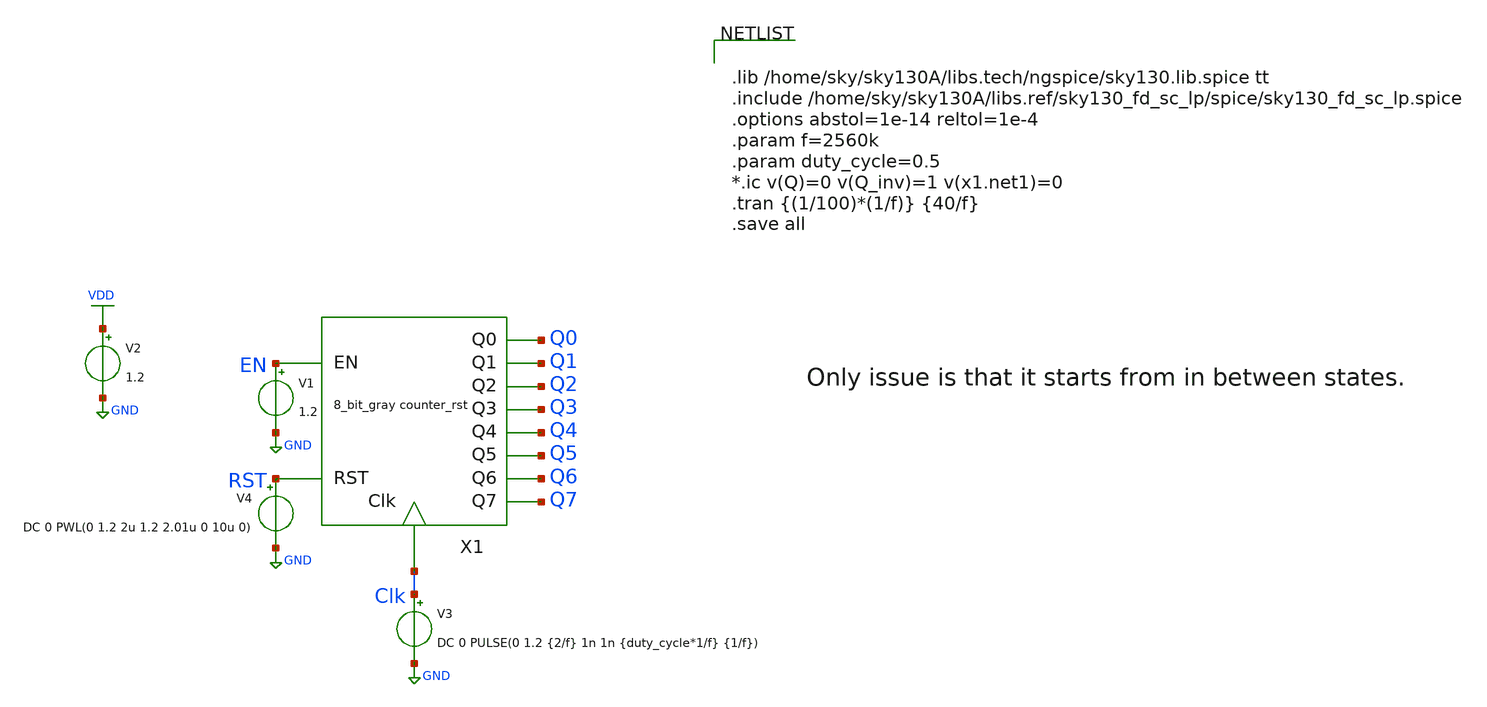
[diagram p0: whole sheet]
** sch_path: xschem/8_bit_gray_counter/8_bit_gray_counter_rst_tb.sch
**.subckt 8_bit_gray_counter_rst_tb
V3 Clk GND DC 0 PULSE(0 1.2 {2/f} 1n 1n {duty_cycle*1/f} {1/f})
V1 EN GND 1.2
V2 VDD GND 1.2
V4 RST GND DC 0 PWL(0 1.2 2u 1.2 2.01u 0 10u 0)
X1 EN Q1 Q6 Clk Q0 Q2 Q3 Q4 Q5 Q7 RST 8_bit_gray_counter_rst
**** begin user architecture code


.lib /home/sky/sky130A/libs.tech/ngspice/sky130.lib.spice tt
.include /home/sky/sky130A/libs.ref/sky130_fd_sc_lp/spice/sky130_fd_sc_lp.spice
.options abstol=1e-14 reltol=1e-4
.param f=2560k
.param duty_cycle=0.5
*.ic v(Q)=0 v(Q_inv)=1 v(x1.net1)=0
.tran {(1/100)*(1/f)} {40/f}
.save all


**** end user architecture code
**.ends
.GLOBAL GND
.GLOBAL VDD
.end
